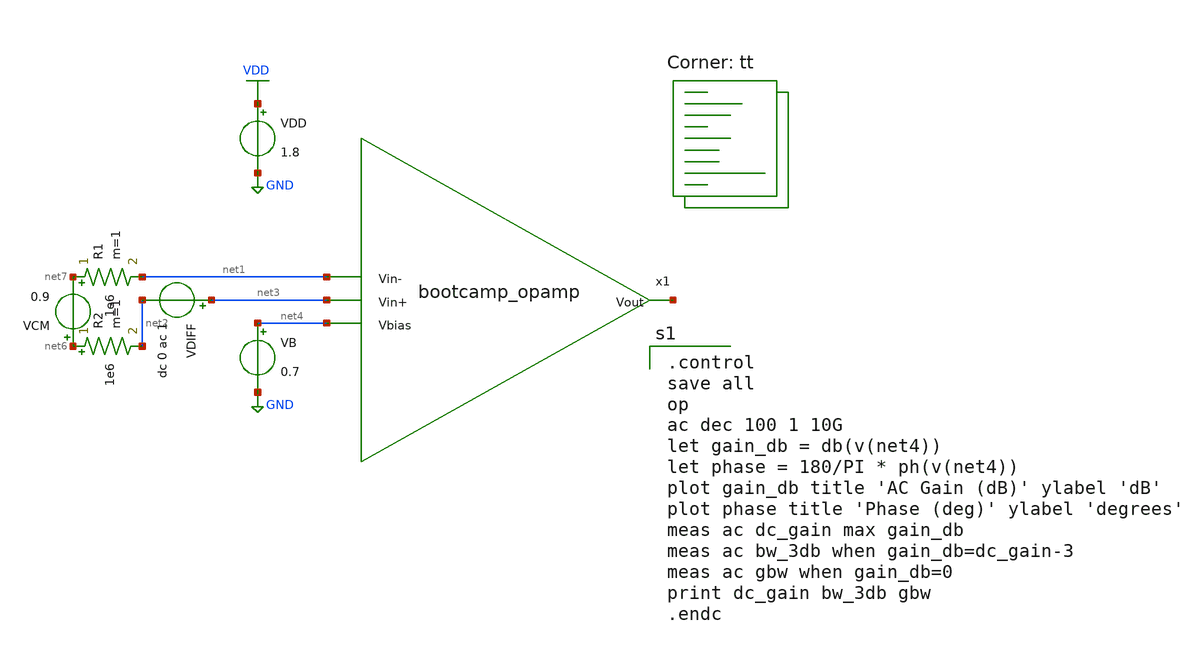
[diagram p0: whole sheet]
** sch_path: analog/schematics/tb_ac_analysis.sch
**.subckt tb_ac_analysis
x1 net5 net1 net3 net4 bootcamp_opamp
VDD VDD GND 1.8
VCM net6 net7 0.9
VB net4 GND 0.7
VDIFF net3 net2 dc 0 ac 1
R1 net7 net1 1e6 m=1
R2 net6 net2 1e6 m=1
**** begin user architecture code

.control
save all
op
ac dec 100 1 10G
let gain_db = db(v(net4))
let phase = 180/PI * ph(v(net4))
plot gain_db title 'AC Gain (dB)' ylabel 'dB'
plot phase title 'Phase (deg)' ylabel 'degrees'
meas ac dc_gain max gain_db
meas ac bw_3db when gain_db=dc_gain-3
meas ac gbw when gain_db=0
print dc_gain bw_3db gbw
.endc

.lib $::SKYWATER_MODELS/sky130.lib.spice tt
**** end user architecture code
**.ends
.GLOBAL GND
.GLOBAL VDD
.end
